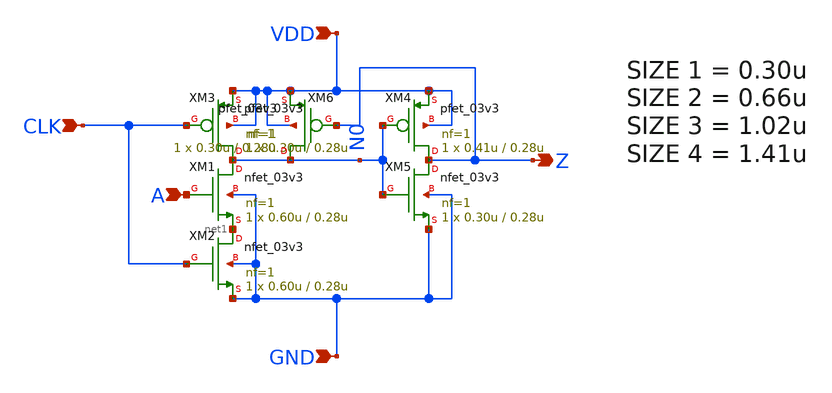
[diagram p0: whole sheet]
** sch_path: xschem/buffer.sch
**.subckt buffer A CLK VDD GND Z
*.ipin A
*.ipin CLK
*.ipin VDD
*.ipin GND
*.opin Z
XM1 N0 A net1 GND nfet_03v3 L=0.28u W=0.60u nf=1 ad='int((nf+1)/2) * W/nf * 0.18u' as='int((nf+2)/2) * W/nf * 0.18u'
+ pd='2*int((nf+1)/2) * (W/nf + 0.18u)' ps='2*int((nf+2)/2) * (W/nf + 0.18u)' nrd='0.18u / W' nrs='0.18u / W'
+ sa=0 sb=0 sd=0 m=1
XM2 net1 CLK GND GND nfet_03v3 L=0.28u W=0.60u nf=1 ad='int((nf+1)/2) * W/nf * 0.18u' as='int((nf+2)/2) * W/nf * 0.18u'
+ pd='2*int((nf+1)/2) * (W/nf + 0.18u)' ps='2*int((nf+2)/2) * (W/nf + 0.18u)' nrd='0.18u / W' nrs='0.18u / W'
+ sa=0 sb=0 sd=0 m=1
XM3 N0 CLK VDD VDD pfet_03v3 L=0.28u W=0.30u nf=1 ad='int((nf+1)/2) * W/nf * 0.18u' as='int((nf+2)/2) * W/nf * 0.18u'
+ pd='2*int((nf+1)/2) * (W/nf + 0.18u)' ps='2*int((nf+2)/2) * (W/nf + 0.18u)' nrd='0.18u / W' nrs='0.18u / W'
+ sa=0 sb=0 sd=0 m=1
XM4 Z N0 VDD VDD pfet_03v3 L=0.28u W=0.41u nf=1 ad='int((nf+1)/2) * W/nf * 0.18u' as='int((nf+2)/2) * W/nf * 0.18u'
+ pd='2*int((nf+1)/2) * (W/nf + 0.18u)' ps='2*int((nf+2)/2) * (W/nf + 0.18u)' nrd='0.18u / W' nrs='0.18u / W'
+ sa=0 sb=0 sd=0 m=1
XM5 Z N0 GND GND nfet_03v3 L=0.28u W=0.30u nf=1 ad='int((nf+1)/2) * W/nf * 0.18u' as='int((nf+2)/2) * W/nf * 0.18u'
+ pd='2*int((nf+1)/2) * (W/nf + 0.18u)' ps='2*int((nf+2)/2) * (W/nf + 0.18u)' nrd='0.18u / W' nrs='0.18u / W'
+ sa=0 sb=0 sd=0 m=1
XM6 N0 Z VDD VDD pfet_03v3 L=0.28u W=0.30u nf=1 ad='int((nf+1)/2) * W/nf * 0.18u' as='int((nf+2)/2) * W/nf * 0.18u'
+ pd='2*int((nf+1)/2) * (W/nf + 0.18u)' ps='2*int((nf+2)/2) * (W/nf + 0.18u)' nrd='0.18u / W' nrs='0.18u / W'
+ sa=0 sb=0 sd=0 m=1
**.ends
.end
